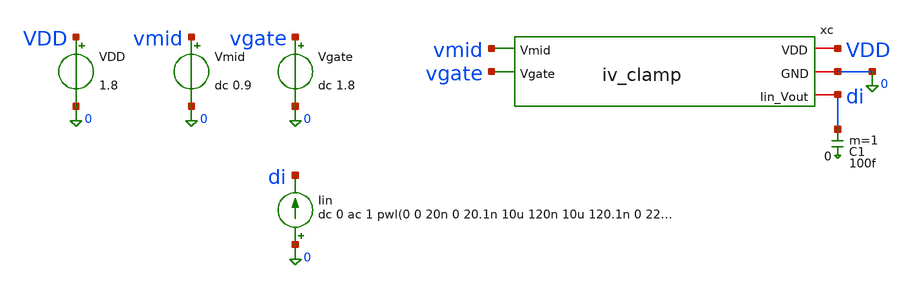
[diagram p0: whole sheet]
** sch_path: sch/summing_stage/iv_clamp_tb.sch
**.subckt iv_clamp_tb
xc VDD 0 vmid vgate di iv_clamp
VDD VDD 0 1.8
.save i(vdd)
Vmid vmid 0 dc 0.9
.save i(vmid)
Vgate vgate 0 dc 1.8
.save i(vgate)
Iin 0 di dc 0 ac 1 pwl(0 0 20n 0 20.1n 10u 120n 10u 120.1n 0 220n 0 220.1n -10u 320n -10u 320.1n 0
+ 420n 0 420.1n 20u 520n 20u 520.1n 0 620n 0 620.1n -20u 720n -20u 720.1n 0 820n 0)
C1 di 0 100f m=1
**** begin user architecture code

** opencircuitdesign pdks install
.lib $::SKYWATER_MODELS/sky130.lib.spice tt
.include $::SKYWATER_STDCELLS/sky130_fd_sc_hd.spice



.options reltol=1e-6
.nodeset v(di)=0.9
.save all
.save i(vmid)
.include iv_clamp_tb.save

.control
  * ---- 1. operating point, Iin = 0 ----
  op
  write @schname\.raw
  let imid = -i(Vmid)
  print v(di) v(vmid) v(vgate) imid > op_f.log
  print @m.xc.xm3.msky130_fd_pr__nfet_01v8[vds] @m.xc.xm3.msky130_fd_pr__nfet_01v8[vdsat]
+ @m.xc.xm3.msky130_fd_pr__nfet_01v8[vth] @m.xc.xm3.msky130_fd_pr__nfet_01v8[gm] @m.xc.xm3.msky130_fd_pr__nfet_01v8[id] >> op_f.log
  print @m.xc.xm2.msky130_fd_pr__pfet_01v8_lvt[vds] @m.xc.xm2.msky130_fd_pr__pfet_01v8_lvt[vdsat]
+ @m.xc.xm2.msky130_fd_pr__pfet_01v8_lvt[vth] @m.xc.xm2.msky130_fd_pr__pfet_01v8_lvt[gm] @m.xc.xm2.msky130_fd_pr__pfet_01v8_lvt[id] >> op_f.log
  print @m.xc.xm1.msky130_fd_pr__pfet_01v8_lvt[vds] @m.xc.xm1.msky130_fd_pr__pfet_01v8_lvt[vdsat]
+ @m.xc.xm1.msky130_fd_pr__pfet_01v8_lvt[vth] @m.xc.xm1.msky130_fd_pr__pfet_01v8_lvt[gm] @m.xc.xm1.msky130_fd_pr__pfet_01v8_lvt[id] >> op_f.log

  * ---- 2. transfer curve V(Iin): fine sweep around zero, then the full range ----
  dc Iin -1u 1u 0.01u
  let vdi = v(di)
  let imid = -i(Vmid)
  wrdata dc_fine.csv vdi imid

  dc Iin -25u 25u 0.05u
  let vdi = v(di)
  let imid = -i(Vmid)
  wrdata dc_i.csv vdi imid

  * ---- 3. V_GATE sweep (outer loop), Iin inner ----
  dc Iin -25u 25u 0.25u Vgate 1.4 1.8 0.05
  let vdi = v(di)
  let imid = -i(Vmid)
  let vvg = v(vgate)
  wrdata dc_vg.csv vdi imid vvg
  alter Vgate dc = 1.8

  * ---- 4. V_MID sweep (outer loop), Iin inner ----
  dc Iin -25u 25u 0.25u Vmid 0.6 1.2 0.05
  let vdi = v(di)
  let imid = -i(Vmid)
  let vvm = v(vmid)
  wrdata dc_vm.csv vdi imid vvm
  alter Vmid dc = 0.9

  * ---- 5. small-signal impedance at three bias currents (ac 1 A on Iin, so v(di) is the impedance
+ in ohm) ----
  alter Iin dc = 0
  ac dec 50 1k 10G
  let zdb = db(v(di))
  let zph = cph(v(di))*180/pi
  wrdata ac_0.csv zdb zph

  alter Iin dc = 5u
  ac dec 50 1k 10G
  let zdb = db(v(di))
  let zph = cph(v(di))*180/pi
  wrdata ac_p5.csv zdb zph

  alter Iin dc = -5u
  ac dec 50 1k 10G
  let zdb = db(v(di))
  let zph = cph(v(di))*180/pi
  wrdata ac_m5.csv zdb zph

  * ---- 6. transient: +/-10 uA and +/-20 uA current steps (the pwl on Iin) ----
  alter Iin dc = 0
  tran 0.1n 820n
  let vdi = v(di)
  wrdata tran.csv vdi
.endc


**** end user architecture code
**.ends

* expanding   symbol:  /foss/designs/sar_adc/sch/summing_stage/iv_clamp.sym # of pins=5
** sym_path: sch/summing_stage/iv_clamp.sym
** sch_path: sch/summing_stage/iv_clamp.sch
.subckt iv_clamp VDD GND Vmid Vgate Iin_Vout
*.ipin Vmid
*.iopin VDD
*.iopin GND
*.ipin Vgate
*.iopin Iin_Vout
XM3 Iin_Vout Vgate Vmid GND sky130_fd_pr__nfet_01v8 L=9 W=6 nf=1 ad='int((1 + 1)/2) * 6 / 1 * 0.29' as='int((1 + 2)/2) * 6 / 1 * 0.29'
+ pd='2*int((1 + 1)/2) * (6 / 1 + 0.29)' ps='2*int((1 + 2)/2) * (6 / 1 + 0.29)' nrd='0.29 / 6 ' nrs='0.29 / 6 '
+ sa=0 sb=0 sd=0 mult=1 m=1
XM1 GND net1 Iin_Vout VDD sky130_fd_pr__pfet_01v8_lvt L=1 W=15 nf=3 ad='int((3 + 1)/2) * 15 / 3 * 0.29'
+ as='int((3 + 2)/2) * 15 / 3 * 0.29' pd='2*int((3 + 1)/2) * (15 / 3 + 0.29)' ps='2*int((3 + 2)/2) * (15 / 3 + 0.29)'
+ nrd='0.29 / 15 ' nrs='0.29 / 15 ' sa=0 sb=0 sd=0 mult=1 m=1
XM2 net1 net1 Vmid Vmid sky130_fd_pr__pfet_01v8_lvt L=1 W=15 nf=3 ad='int((3 + 1)/2) * 15 / 3 * 0.29'
+ as='int((3 + 2)/2) * 15 / 3 * 0.29' pd='2*int((3 + 1)/2) * (15 / 3 + 0.29)' ps='2*int((3 + 2)/2) * (15 / 3 + 0.29)'
+ nrd='0.29 / 15 ' nrs='0.29 / 15 ' sa=0 sb=0 sd=0 mult=1 m=1
Ib net1 GND 500n
.ends

.end
